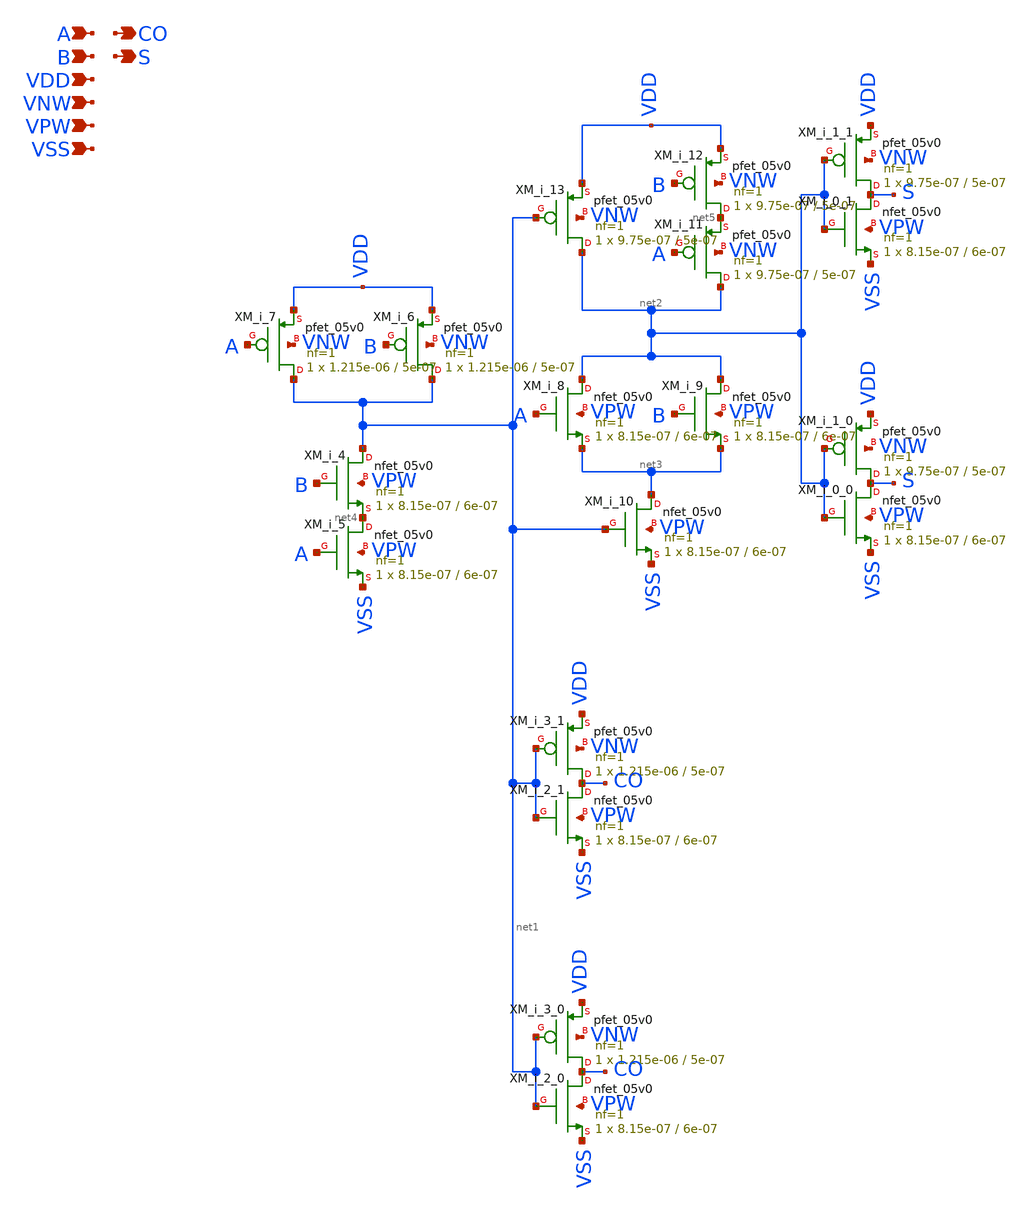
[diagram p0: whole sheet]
** sch_path: schematics/addh/gf180mcu_fd_sc_mcu7t5v0__addh_2.sch
**.subckt gf180mcu_fd_sc_mcu7t5v0__addh_2 A B CO S VDD VNW VPW VSS
*.ipin A
*.ipin B
*.opin CO
*.opin S
*.ipin VDD
*.ipin VNW
*.ipin VPW
*.ipin VSS
XM_i_3_1 CO net1 VDD VNW pfet_05v0 L=5e-07 W=1.215e-06 nf=1 ad='int((nf+1)/2) * W/nf * 0.18u' as='int((nf+2)/2) * W/nf * 0.18u'
+ pd='2*int((nf+1)/2) * (W/nf + 0.18u)' ps='2*int((nf+2)/2) * (W/nf + 0.18u)' nrd='0.18u / W' nrs='0.18u / W'
+ sa=0 sb=0 sd=0 m=1 par=1
XM_i_2_1 CO net1 VSS VPW nfet_05v0 L=6e-07 W=8.15e-07 nf=1 ad='int((nf+1)/2) * W/nf * 0.18u' as='int((nf+2)/2) * W/nf * 0.18u'
+ pd='2*int((nf+1)/2) * (W/nf + 0.18u)' ps='2*int((nf+2)/2) * (W/nf + 0.18u)' nrd='0.18u / W' nrs='0.18u / W'
+ sa=0 sb=0 sd=0 m=1
XM_i_3_0 CO net1 VDD VNW pfet_05v0 L=5e-07 W=1.215e-06 nf=1 ad='int((nf+1)/2) * W/nf * 0.18u' as='int((nf+2)/2) * W/nf * 0.18u'
+ pd='2*int((nf+1)/2) * (W/nf + 0.18u)' ps='2*int((nf+2)/2) * (W/nf + 0.18u)' nrd='0.18u / W' nrs='0.18u / W'
+ sa=0 sb=0 sd=0 m=1 par=1
XM_i_2_0 CO net1 VSS VPW nfet_05v0 L=6e-07 W=8.15e-07 nf=1 ad='int((nf+1)/2) * W/nf * 0.18u' as='int((nf+2)/2) * W/nf * 0.18u'
+ pd='2*int((nf+1)/2) * (W/nf + 0.18u)' ps='2*int((nf+2)/2) * (W/nf + 0.18u)' nrd='0.18u / W' nrs='0.18u / W'
+ sa=0 sb=0 sd=0 m=1
XM_i_7 net1 A VDD VNW pfet_05v0 L=5e-07 W=1.215e-06 nf=1 ad='int((nf+1)/2) * W/nf * 0.18u' as='int((nf+2)/2) * W/nf * 0.18u'
+ pd='2*int((nf+1)/2) * (W/nf + 0.18u)' ps='2*int((nf+2)/2) * (W/nf + 0.18u)' nrd='0.18u / W' nrs='0.18u / W'
+ sa=0 sb=0 sd=0 m=1 par=1
XM_i_6 net1 B VDD VNW pfet_05v0 L=5e-07 W=1.215e-06 nf=1 ad='int((nf+1)/2) * W/nf * 0.18u' as='int((nf+2)/2) * W/nf * 0.18u'
+ pd='2*int((nf+1)/2) * (W/nf + 0.18u)' ps='2*int((nf+2)/2) * (W/nf + 0.18u)' nrd='0.18u / W' nrs='0.18u / W'
+ sa=0 sb=0 sd=0 m=1 par=1
XM_i_4 net1 B net4 VPW nfet_05v0 L=6e-07 W=8.15e-07 nf=1 ad='int((nf+1)/2) * W/nf * 0.18u' as='int((nf+2)/2) * W/nf * 0.18u'
+ pd='2*int((nf+1)/2) * (W/nf + 0.18u)' ps='2*int((nf+2)/2) * (W/nf + 0.18u)' nrd='0.18u / W' nrs='0.18u / W'
+ sa=0 sb=0 sd=0 m=1
XM_i_5 net4 A VSS VPW nfet_05v0 L=6e-07 W=8.15e-07 nf=1 ad='int((nf+1)/2) * W/nf * 0.18u' as='int((nf+2)/2) * W/nf * 0.18u'
+ pd='2*int((nf+1)/2) * (W/nf + 0.18u)' ps='2*int((nf+2)/2) * (W/nf + 0.18u)' nrd='0.18u / W' nrs='0.18u / W'
+ sa=0 sb=0 sd=0 m=1
XM_i_13 net2 net1 VDD VNW pfet_05v0 L=5e-07 W=9.75e-07 nf=1 ad='int((nf+1)/2) * W/nf * 0.18u' as='int((nf+2)/2) * W/nf * 0.18u'
+ pd='2*int((nf+1)/2) * (W/nf + 0.18u)' ps='2*int((nf+2)/2) * (W/nf + 0.18u)' nrd='0.18u / W' nrs='0.18u / W'
+ sa=0 sb=0 sd=0 m=1 par=1
XM_i_12 net5 B VDD VNW pfet_05v0 L=5e-07 W=9.75e-07 nf=1 ad='int((nf+1)/2) * W/nf * 0.18u' as='int((nf+2)/2) * W/nf * 0.18u'
+ pd='2*int((nf+1)/2) * (W/nf + 0.18u)' ps='2*int((nf+2)/2) * (W/nf + 0.18u)' nrd='0.18u / W' nrs='0.18u / W'
+ sa=0 sb=0 sd=0 m=1 par=1
XM_i_11 net2 A net5 VNW pfet_05v0 L=5e-07 W=9.75e-07 nf=1 ad='int((nf+1)/2) * W/nf * 0.18u' as='int((nf+2)/2) * W/nf * 0.18u'
+ pd='2*int((nf+1)/2) * (W/nf + 0.18u)' ps='2*int((nf+2)/2) * (W/nf + 0.18u)' nrd='0.18u / W' nrs='0.18u / W'
+ sa=0 sb=0 sd=0 m=1 par=1
XM_i_8 net2 A net3 VPW nfet_05v0 L=6e-07 W=8.15e-07 nf=1 ad='int((nf+1)/2) * W/nf * 0.18u' as='int((nf+2)/2) * W/nf * 0.18u'
+ pd='2*int((nf+1)/2) * (W/nf + 0.18u)' ps='2*int((nf+2)/2) * (W/nf + 0.18u)' nrd='0.18u / W' nrs='0.18u / W'
+ sa=0 sb=0 sd=0 m=1
XM_i_9 net2 B net3 VPW nfet_05v0 L=6e-07 W=8.15e-07 nf=1 ad='int((nf+1)/2) * W/nf * 0.18u' as='int((nf+2)/2) * W/nf * 0.18u'
+ pd='2*int((nf+1)/2) * (W/nf + 0.18u)' ps='2*int((nf+2)/2) * (W/nf + 0.18u)' nrd='0.18u / W' nrs='0.18u / W'
+ sa=0 sb=0 sd=0 m=1
XM_i_10 net3 net1 VSS VPW nfet_05v0 L=6e-07 W=8.15e-07 nf=1 ad='int((nf+1)/2) * W/nf * 0.18u' as='int((nf+2)/2) * W/nf * 0.18u'
+ pd='2*int((nf+1)/2) * (W/nf + 0.18u)' ps='2*int((nf+2)/2) * (W/nf + 0.18u)' nrd='0.18u / W' nrs='0.18u / W'
+ sa=0 sb=0 sd=0 m=1
XM_i_1_1 S net2 VDD VNW pfet_05v0 L=5e-07 W=9.75e-07 nf=1 ad='int((nf+1)/2) * W/nf * 0.18u' as='int((nf+2)/2) * W/nf * 0.18u'
+ pd='2*int((nf+1)/2) * (W/nf + 0.18u)' ps='2*int((nf+2)/2) * (W/nf + 0.18u)' nrd='0.18u / W' nrs='0.18u / W'
+ sa=0 sb=0 sd=0 m=1 par=1
XM_i_0_1 S net2 VSS VPW nfet_05v0 L=6e-07 W=8.15e-07 nf=1 ad='int((nf+1)/2) * W/nf * 0.18u' as='int((nf+2)/2) * W/nf * 0.18u'
+ pd='2*int((nf+1)/2) * (W/nf + 0.18u)' ps='2*int((nf+2)/2) * (W/nf + 0.18u)' nrd='0.18u / W' nrs='0.18u / W'
+ sa=0 sb=0 sd=0 m=1
XM_i_1_0 S net2 VDD VNW pfet_05v0 L=5e-07 W=9.75e-07 nf=1 ad='int((nf+1)/2) * W/nf * 0.18u' as='int((nf+2)/2) * W/nf * 0.18u'
+ pd='2*int((nf+1)/2) * (W/nf + 0.18u)' ps='2*int((nf+2)/2) * (W/nf + 0.18u)' nrd='0.18u / W' nrs='0.18u / W'
+ sa=0 sb=0 sd=0 m=1 par=1
XM_i_0_0 S net2 VSS VPW nfet_05v0 L=6e-07 W=8.15e-07 nf=1 ad='int((nf+1)/2) * W/nf * 0.18u' as='int((nf+2)/2) * W/nf * 0.18u'
+ pd='2*int((nf+1)/2) * (W/nf + 0.18u)' ps='2*int((nf+2)/2) * (W/nf + 0.18u)' nrd='0.18u / W' nrs='0.18u / W'
+ sa=0 sb=0 sd=0 m=1
**.ends
.end
